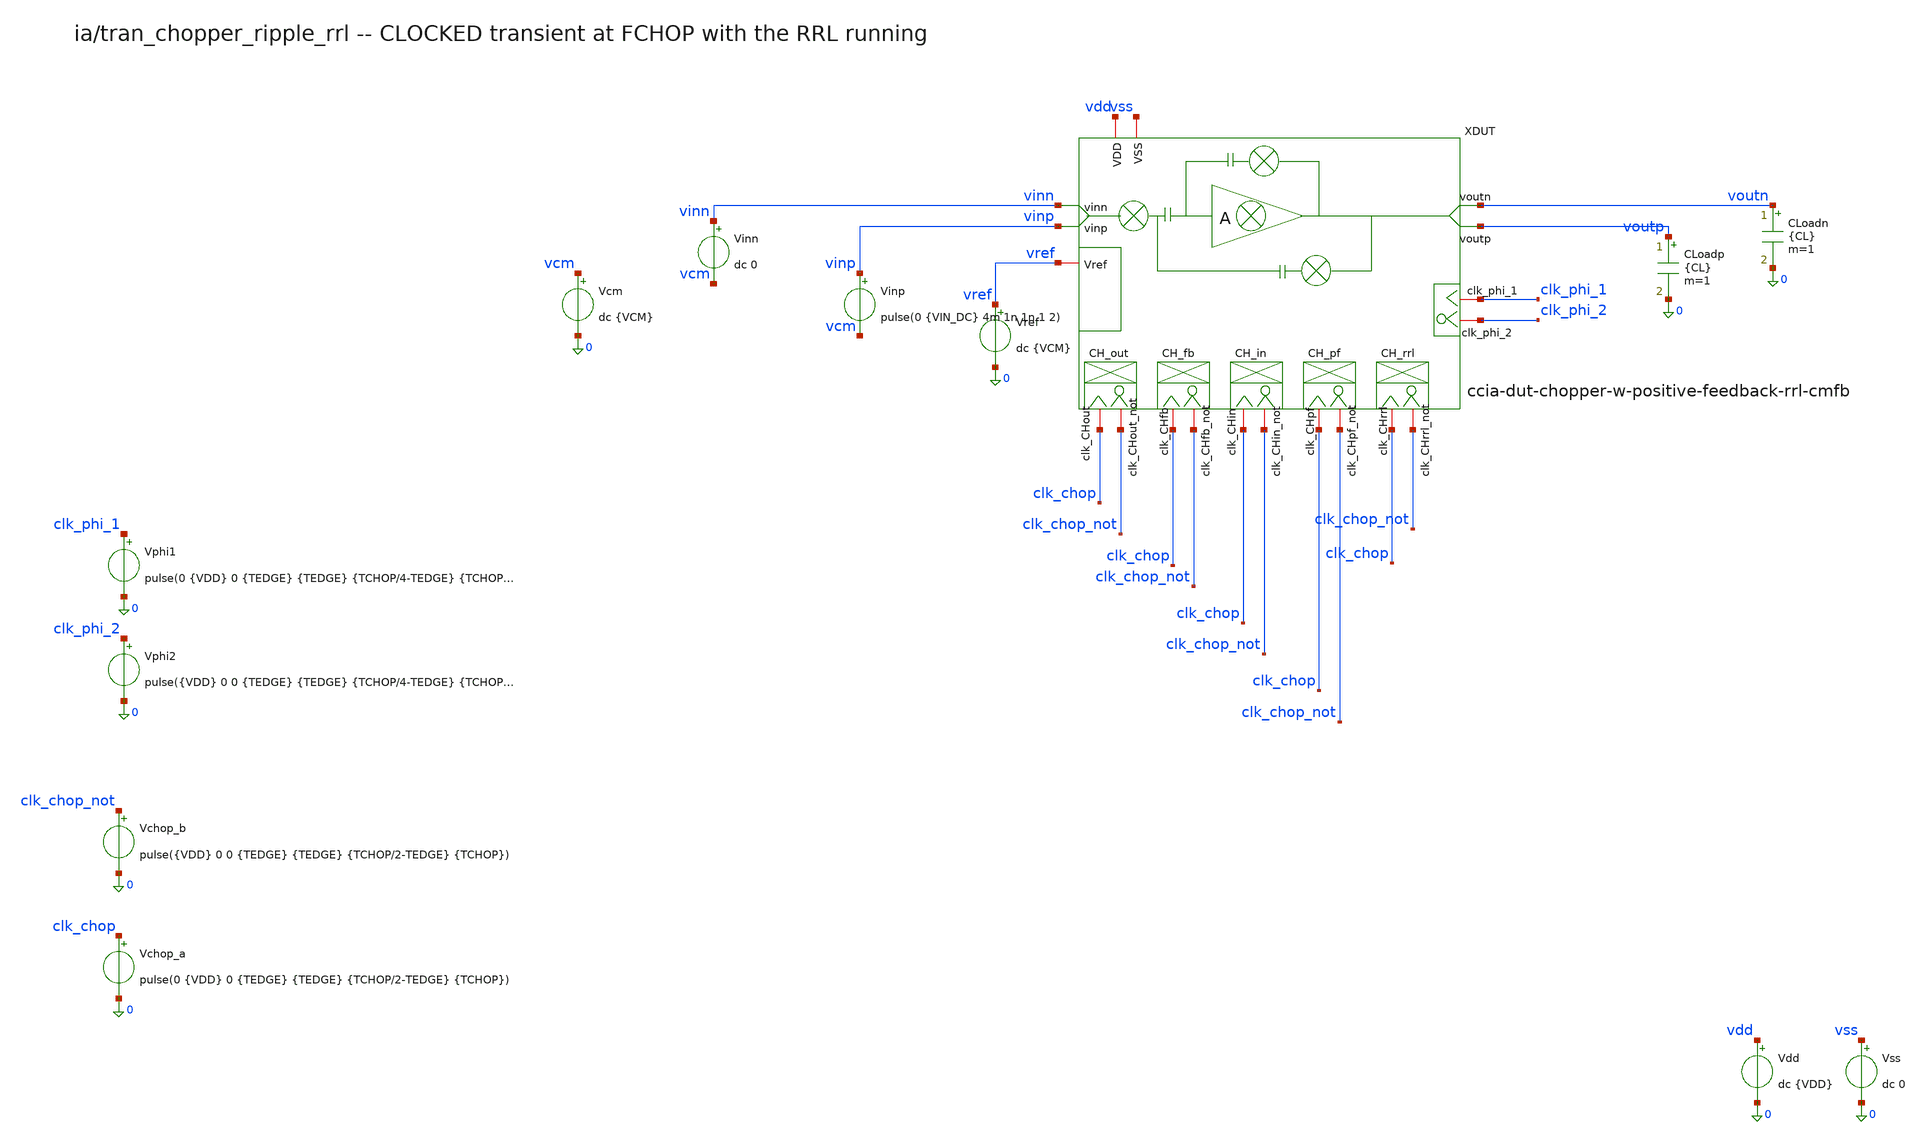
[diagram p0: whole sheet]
** sch_path: analog-db/drawings/ccia-02-QinwenFan-chopper-ripple-reduction/testbenches/ccia-dut/tran_chopper_ripple_rrl_cmfb.sch
* Copyright 2026 MacAnalog Research Group
**.subckt tran_chopper_ripple_rrl_cmfb
XDUT clk_chop clk_chop_not clk_chop clk_chop_not vref voutn vinn vinp voutp clk_chop clk_chop_not
+ vdd vss clk_chop clk_chop_not clk_chop clk_chop_not clk_phi_1 clk_phi_2
+ ccia-dut-chopper-w-positive-feedback-rrl-cmfb
Vdd vdd 0 dc {VDD}
Vss vss 0 dc 0
Vchop_a clk_chop 0 pulse(0 {VDD} 0 {TEDGE} {TEDGE} {TCHOP/2-TEDGE} {TCHOP})
Vchop_b clk_chop_not 0 pulse({VDD} 0 0 {TEDGE} {TEDGE} {TCHOP/2-TEDGE} {TCHOP})
Vphi1 clk_phi_1 0 pulse(0 {VDD} 0 {TEDGE} {TEDGE} {TCHOP/4-TEDGE} {TCHOP/2})
Vphi2 clk_phi_2 0 pulse({VDD} 0 0 {TEDGE} {TEDGE} {TCHOP/4-TEDGE} {TCHOP/2})
Vref vref 0 dc {VCM}
Vcm vcm 0 dc {VCM}
Vinp vinp vcm pulse(0 {VIN_DC} 4m 1n 1n 1 2)
Vinn vinn vcm dc 0
CLoadp voutp 0 {CL} m=1
CLoadn voutn 0 {CL} m=1
**** begin user architecture code


* TESTBENCH tran_chopper_ripple_rrl_cmfb -- DUT ccia-dut-chopper-w-positive-feedback-rrl-cmfb
* produces: v_ripple_pp, v_ripple0_pp, gain_cl, vos_residual
* recorded baseline: no ia_004 baseline -- the composite has NO CMFB, so the output CM rails once
*+ the SC clocks run. ia_002 (no RRL) records v_ripple_pp 0.4022486 V; ia_003 (PF, no RRL) 0.2198775 V.
* bench bindings (circuits/ia_004_fan_chopper_rrl/analyses/)
.param VDD=1.2
.param VCM=0.6
.param CL=50f
.param FCHOP=5k
.param TEDGE=50n
.param VIN_DC=10m
.param TCHOP={1/FCHOP}




* CCIA top level -- ccia-dut-chopper-w-positive-feedback-rrl.sch
* source: circuits/ia_004_fan_chopper_rrl/pdk/ihp-sg13g2/sizing.yaml
.param x_dut_cin1_main_value=16p  x_dut_cfb1_main_value=0.8p
.param x_dut_rb1_main_value=10Meg
* Cpf has no ia_004 knob (that composite drops the PF chopper); this drawing
* keeps it, so take ia_003_fan_chopper_pf's authored value.
.param x_dut_cpf1_main_value=0.8p
* --- behavioural-ideal CMFB servo --------------------------------------
* Built from primitives (Rm_p/Rm_n + E_cmfb) rather than
* shared/ideal/cmfb-output-ideal-amp-inv.sym, because that block's inner
* ideal-amp-fully-diff uses BARE param names (gm_val/rout_val) which the RRL
* instance already owns -- the servo gain could not be set independently.
*   vcm_ref   commanded output common mode
*   cmfb_rm   CM detector sense resistors (5Meg, not the 1Meg default: this core
*             is a true OTA with high Zout and the detector sits on voutp/voutn)
*   cmfb_gain servo gain A. Plant dvocm/dvb1 ~ 115 V/V, so A=10 gives loop gain
*             ~1150. A=100 SATURATES the servo and the output rails to 1.2 V
*             (measured) -- the amp_030 'stable spurious railed equilibrium'.
.param vcm_ref=0.6097
.param cmfb_rm=5Meg
* TUNED VIA ac_cm_reg (not via transient survival time). Valid points only --
* an AC sweep about a RAILED bias is meaningless, and A=30 rails (vocm 1.193):
*   A    Co     zcm_lf    peaking_db   dc vocm
*   30   any    ~2.98k    ~0.02        1.193  RAILED - numbers are garbage
*   10   10n    27.2      43.2         0.6097
*   10   1u     2.51k      7.05        0.6097
*   10   10u   14.83k      0.23        0.6097
*   3    1u     7.17k      2.42        0.6097  <- picked: passes <=6 dB, stiffest
*   3    10u   22.60k      0.00        0.6097  barely better than open loop
* Open loop (no CMFB) is zcm_lf 28.15k with 0.00 dB peaking.
.param cmfb_gain=3
* servo dominant pole f_p = 1/(2*pi*cmfb_ro*cmfb_co) ~ 16 Hz. Without a pole the
* VCVS is pure gain, the CM loop never rolls off and it oscillates (the clocked
* run died at 78 ns with vocm ringing 0.44<->0.78 V).
* Stability grid on a 200 us clocked run (A x cmfb_co):
*        160p     1n      10n
*   A=10  1.7e-5  3.2e-5  COMPLETES
*   A=3   1.3e-5  COMPLETES COMPLETES
*   A=1   7.0e-5  4.5e-5  COMPLETES
* A=10/10n picked: it completes AND keeps the most loop gain.
.param cmfb_ro=1Meg
.param cmfb_co=1u
.param vb1_main=0.5 vb2_main=0.75 vb3_main=0.45 vb4_main=0.55




* CCIA core opamp -- two-stage-opamp-core[-w-stage-breakout].sch
* (= circuits/amp_026_fan_chopper_ota, namespaced _MAIN in the composite)
.param x_dut_xm1_main_w=20u x_dut_xm1_main_l=1u
.param x_dut_xm2_main_w=20u x_dut_xm2_main_l=0.5u
.param x_dut_xm3_main_w=20u x_dut_xm3_main_l=0.5u
.param x_dut_xm4_main_w=4.7u x_dut_xm4_main_l=1u
.param x_dut_xm5_main_w=4.7u x_dut_xm5_main_l=1u
.param x_dut_xm6_main_w=10u x_dut_xm6_main_l=1u
.param x_dut_xm7_main_w=10u x_dut_xm7_main_l=1u
.param x_dut_xm8_main_w=6.2u x_dut_xm8_main_l=1u
.param x_dut_xm9_main_w=6.2u x_dut_xm9_main_l=1u
.param x_dut_xm10_main_w=10u x_dut_xm10_main_l=0.3u
.param x_dut_xm11_main_w=10u x_dut_xm11_main_l=0.3u
.param x_dut_xm12_main_w=5u x_dut_xm12_main_l=0.3u
.param x_dut_xm13_main_w=5u x_dut_xm13_main_l=0.3u
.param x_dut_xm14_main_w=6u x_dut_xm14_main_l=0.5u
.param x_dut_xm15_main_w=6u x_dut_xm15_main_l=0.5u
* Miller compensation cap
.param x_dut_cm1_main_value=1p




* RRL switched-capacitor network -- rrl-switched-capa-integrator.sch
* (= circuits/sup_003_rrl_sc_integrator, namespaced _RRL)
.param x_dut_cs1_rrl_value=1p  x_dut_caz1_rrl_value=1p  x_dut_cint1_rrl_value=4p
.param vb1_rrl=0.45 vb2_rrl=0.75 vb3_rrl=0.55 vcmfb_rrl=0.6
* behavioural compensation cell (shared/ideal/ideal-amp-fully-diff.sch).
* gm_val is ia_004's parent override (10u, not sup_003's own 100u): at the
* registry 5 kHz default the un-scaled Gm makes the discrete-time RRL loop
* gain > 1 and the clocked transient diverges.
.param gm_val=10u rout_val=10Meg cout_val=100f
.param rin_val=1T cin_val=10f




* RRL integrator opamp -- integrator-switchcap-opamp.sch
* (= circuits/amp_027_fan_rrl_ota, namespaced _OPAMP_RRL)
.param x_dut_xm1_opamp_rrl_w=20u x_dut_xm1_opamp_rrl_l=1u
.param x_dut_xm2_opamp_rrl_w=20u x_dut_xm2_opamp_rrl_l=0.5u
.param x_dut_xm3_opamp_rrl_w=20u x_dut_xm3_opamp_rrl_l=0.5u
.param x_dut_xm4_opamp_rrl_w=10u x_dut_xm4_opamp_rrl_l=1u
.param x_dut_xm5_opamp_rrl_w=4u x_dut_xm5_opamp_rrl_l=0.5u
.param x_dut_xm6_opamp_rrl_w=4u x_dut_xm6_opamp_rrl_l=0.5u
.param x_dut_xm7_opamp_rrl_w=4u x_dut_xm7_opamp_rrl_l=0.5u
.param x_dut_xm8_opamp_rrl_w=4u x_dut_xm8_opamp_rrl_l=0.5u
.param x_dut_xm9_opamp_rrl_w=10u x_dut_xm9_opamp_rrl_l=0.3u
.param x_dut_xm10_opamp_rrl_w=10u x_dut_xm10_opamp_rrl_l=0.3u
.param x_dut_xm11_opamp_rrl_w=5u x_dut_xm11_opamp_rrl_l=0.3u
.param x_dut_xm12_opamp_rrl_w=5u x_dut_xm12_opamp_rrl_l=0.3u
.param x_dut_xm13_opamp_rrl_w=6u x_dut_xm13_opamp_rrl_l=1u
.param x_dut_xm14_opamp_rrl_w=6u x_dut_xm14_opamp_rrl_l=1u
.param x_dut_xm15_opamp_rrl_w=2u x_dut_xm15_opamp_rrl_l=1u
.param x_dut_xm16_opamp_rrl_w=2u x_dut_xm16_opamp_rrl_l=1u




* Switches -- shared/transmission_gate_pair.sch, used by EVERY chopper
* (in/fb/out/pf/rrl) and by the RRL's SC switches.
* Held at the PDK geometry floor and deliberately NOT sized yet.
.param tg_n_w=0.18u tg_n_l=0.13u
.param tg_p_w=0.18u tg_p_l=0.13u




.control
  save v(voutp) v(voutn) v(vinp) v(vinn) v(vref) v(clk_chop) v(clk_phi_1) i(Vdd)
  set hcopydevtype=svg
  set filetype=binary
  tran 1u 8m 0 200n
  let vd = v(voutp) - v(voutn)
  let vodm = vd
  let vocm = (v(voutp) + v(voutn))/2
  meas tran vavga AVG vd from=3m to=4m
  meas tran vavgb AVG vd from=7m to=8m
  meas tran vdmax MAX vd from=7m to=8m
  meas tran vdmin MIN vd from=7m to=8m
  meas tran vdmax0 MAX vd from=3m to=4m
  meas tran vdmin0 MIN vd from=3m to=4m
  let v_ripple_pp = vdmax - vdmin
  let v_ripple0_pp = vdmax0 - vdmin0
  let gain_cl = (vavgb - vavga)/10m
  let vos_residual = vavga/gain_cl
  print v_ripple_pp v_ripple0_pp gain_cl vos_residual
  * CM DIAGNOSTIC: this core has no CMFB, so the run usually dies of output-CM
  * runaway rather than of anything differential. A vocm that has left VCM (and a
  * vavg* that has collapsed to ~0) means the ripple figures above describe a
  * railed, dead output - not a working amplifier. See CMFB_PLAN.md.
  meas tran vocm_a AVG vocm from=3m to=4m
  meas tran vocm_max MAX vocm
  meas tran vocm_min MIN vocm
  print vocm_a vocm_max vocm_min
  write tran_chopper_ripple_rrl_cmfb.raw
  * --- waveform output ---------------------------------------
  * hardcopy -> SVG, works in batch. plot -> interactive only.
  hardcopy tran_chopper_ripple_rrl_cmfb_vodm.svg vodm
  hardcopy tran_chopper_ripple_rrl_cmfb_cm.svg v(voutp) v(voutn) vocm
  plot vodm
  plot v(voutp) v(voutn) vocm
.endc




.lib cornerMOSlv.lib mos_tt
.lib cornerRES.lib res_typ
.lib cornerCAP.lib cap_typ
.temp 27


**** end user architecture code
**.ends
.end
